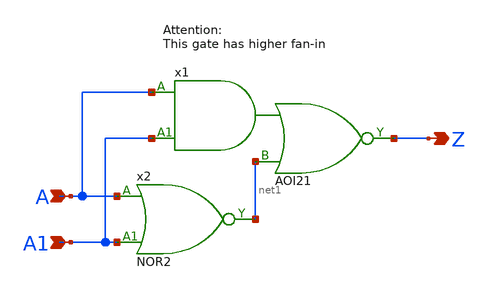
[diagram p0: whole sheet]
** sch_path: Sources/macros/XOR2.sch
**.subckt XOR2 A A1 Z
*.ipin A
*.ipin A1
*.opin Z
x1 A A1 net1 Z VDD GND AOI21 Wmin=1.5u Lmin=1u g=2 m=1
x2 A A1 net1 VDD GND NOR2 Wmin=1.5u Lmin=1u g=2 m=1
**.ends
.end
